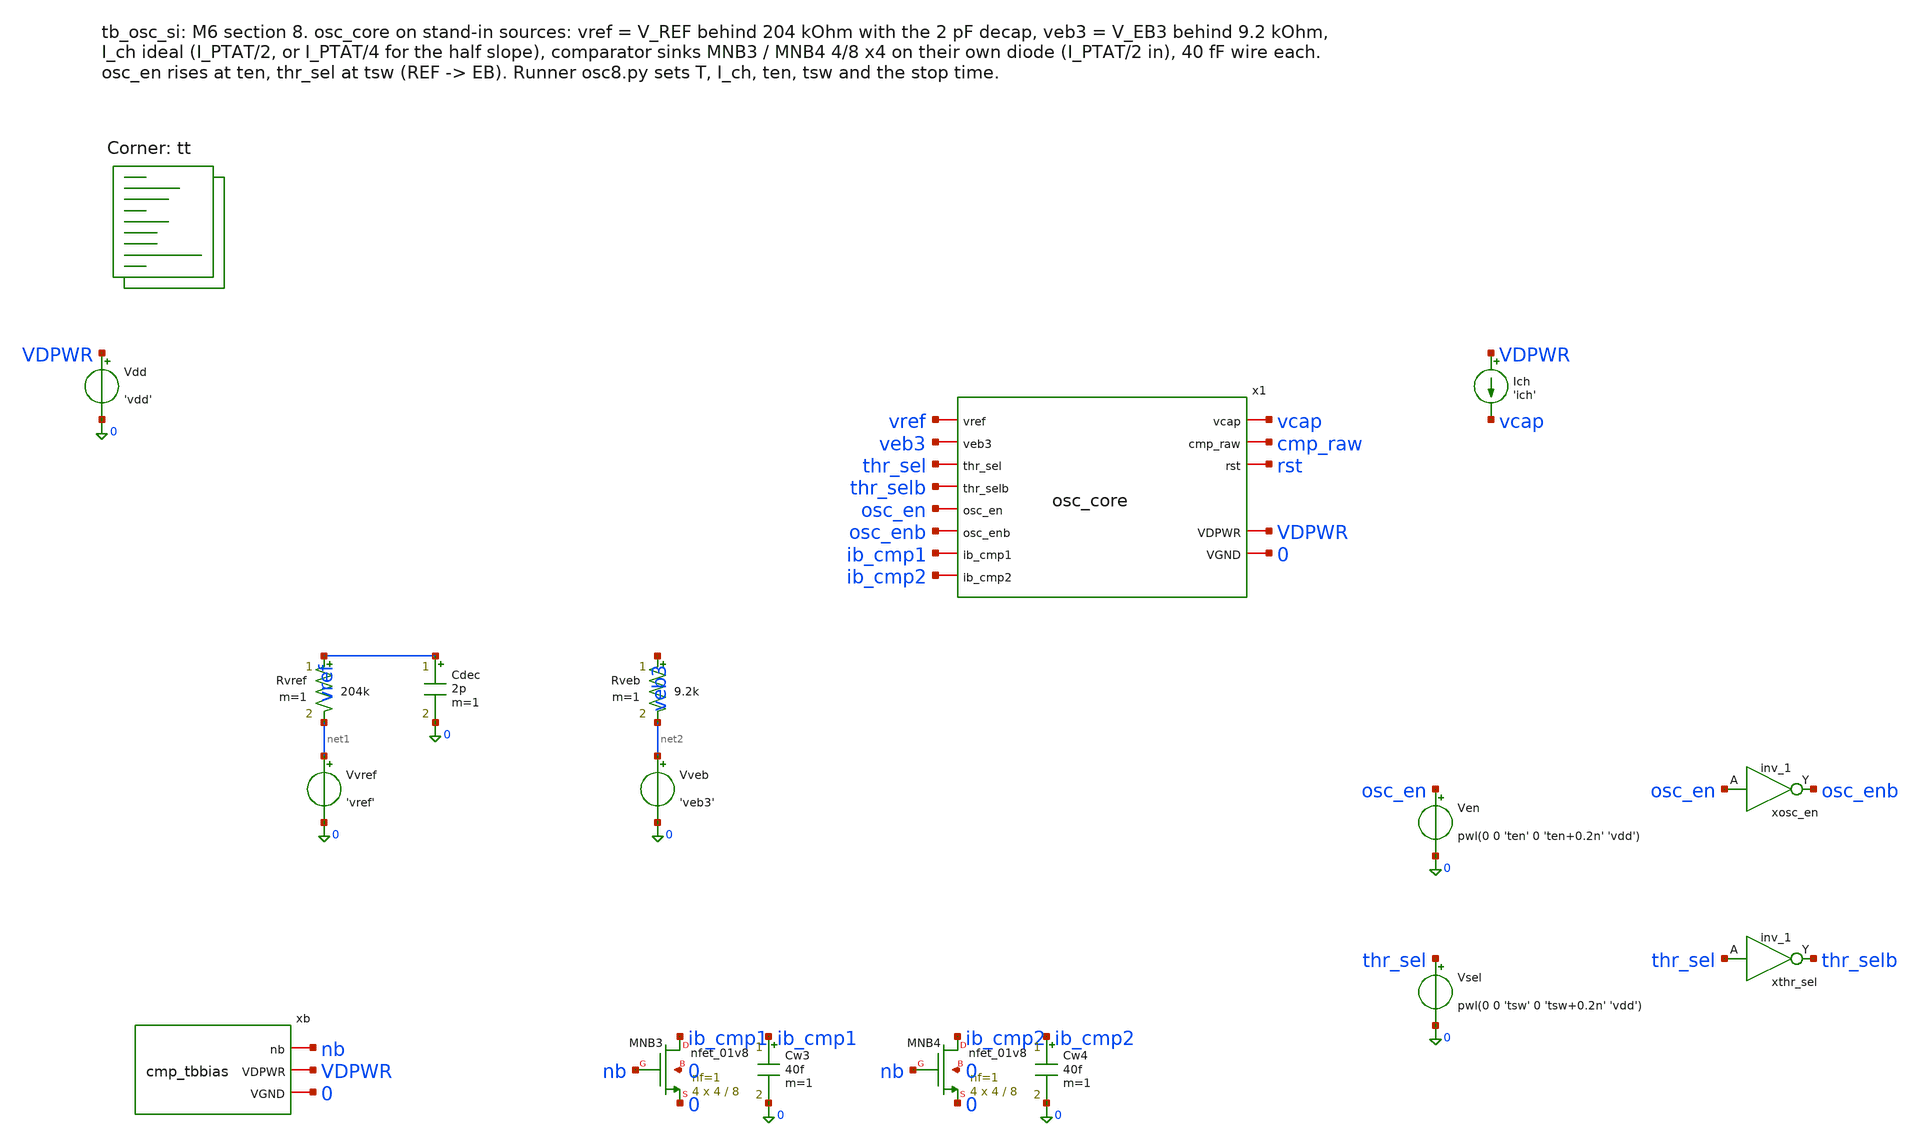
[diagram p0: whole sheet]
** sch_path: xschem/tb_osc_si.sch
**.subckt tb_osc_si
x1 vref veb3 thr_sel thr_selb osc_en osc_enb ib_cmp1 ib_cmp2 vcap cmp_raw rst VDPWR 0 osc_core
Ich VDPWR vcap 'ich'
Vdd VDPWR 0 'vdd'
Vvref net1 0 'vref'
Rvref vref net1 204k m=1
Cdec vref 0 2p m=1
Vveb net2 0 'veb3'
Rveb veb3 net2 9.2k m=1
xb nb VDPWR 0 cmp_tbbias
XMNB3 ib_cmp1 nb 0 0 sky130_fd_pr__nfet_01v8 L=8 W=4 nf=1 ad='int((1 + 1)/2) * 4 / 1 * 0.29' as='int((1 + 2)/2) * 4 / 1 * 0.29'
+ pd='2*int((1 + 1)/2) * (4 / 1 + 0.29)' ps='2*int((1 + 2)/2) * (4 / 1 + 0.29)' nrd='0.29 / 4 ' nrs='0.29 / 4 '
+ sa=0 sb=0 sd=0 mult=4 m=4
Cw3 ib_cmp1 0 40f m=1
XMNB4 ib_cmp2 nb 0 0 sky130_fd_pr__nfet_01v8 L=8 W=4 nf=1 ad='int((1 + 1)/2) * 4 / 1 * 0.29' as='int((1 + 2)/2) * 4 / 1 * 0.29'
+ pd='2*int((1 + 1)/2) * (4 / 1 + 0.29)' ps='2*int((1 + 2)/2) * (4 / 1 + 0.29)' nrd='0.29 / 4 ' nrs='0.29 / 4 '
+ sa=0 sb=0 sd=0 mult=4 m=4
Cw4 ib_cmp2 0 40f m=1
Ven osc_en 0 pwl(0 0 'ten' 0 'ten+0.2n' 'vdd')
xosc_en osc_en 0 0 VDPWR VDPWR osc_enb sky130_fd_sc_hd__inv_1
Vsel thr_sel 0 pwl(0 0 'tsw' 0 'tsw+0.2n' 'vdd')
xthr_sel thr_sel 0 0 VDPWR VDPWR thr_selb sky130_fd_sc_hd__inv_1
**** begin user architecture code
.lib $::SKYWATER_MODELS/sky130.lib.spice tt

.param vdd=1.8 vref=1.24324 veb3=0.709608 ich=1.385555u ten=2u tsw=65.3u
.include /foss/pdks/sky130A/libs.ref/sky130_fd_sc_hd/spice/sky130_fd_sc_hd.spice
.temp 25
.option method=gear
.control
save vcap x1.vthr rst cmp_raw x1.xos.sw
tran 0.2n 140u 0 0.2n
let tdr = 48u
let tde = 98u
meas tran r1 when v(rst)=0.9 rise=1
print r1
meas tran r2 when v(rst)=0.9 rise=2
print r2
meas tran r3 when v(rst)=0.9 rise=3
print r3
meas tran r4 when v(rst)=0.9 rise=4
print r4
meas tran r5 when v(rst)=0.9 rise=5
print r5
meas tran r6 when v(rst)=0.9 rise=6
print r6
meas tran r7 when v(rst)=0.9 rise=7
print r7
meas tran r8 when v(rst)=0.9 rise=8
print r8
meas tran r9 when v(rst)=0.9 rise=9
print r9
meas tran r10 when v(rst)=0.9 rise=10
print r10
meas tran r11 when v(rst)=0.9 rise=11
print r11
meas tran r12 when v(rst)=0.9 rise=12
print r12
meas tran r13 when v(rst)=0.9 rise=13
print r13
meas tran r14 when v(rst)=0.9 rise=14
print r14
meas tran r15 when v(rst)=0.9 rise=15
print r15
meas tran r16 when v(rst)=0.9 rise=16
print r16
meas tran r17 when v(rst)=0.9 rise=17
print r17
meas tran r18 when v(rst)=0.9 rise=18
print r18
meas tran r19 when v(rst)=0.9 rise=19
print r19
meas tran r20 when v(rst)=0.9 rise=20
print r20
meas tran r21 when v(rst)=0.9 rise=21
print r21
meas tran r22 when v(rst)=0.9 rise=22
print r22
meas tran r23 when v(rst)=0.9 rise=23
print r23
meas tran r24 when v(rst)=0.9 rise=24
print r24
meas tran r25 when v(rst)=0.9 rise=25
print r25
meas tran r26 when v(rst)=0.9 rise=26
print r26
meas tran r27 when v(rst)=0.9 rise=27
print r27
meas tran r28 when v(rst)=0.9 rise=28
print r28
meas tran r29 when v(rst)=0.9 rise=29
print r29
meas tran r30 when v(rst)=0.9 rise=30
print r30
meas tran r31 when v(rst)=0.9 rise=31
print r31
meas tran r32 when v(rst)=0.9 rise=32
print r32
meas tran tc when v(vcap)=v(x1.vthr) rise=1 td=$&tdr
meas tran tcmp when v(cmp_raw)=0.9 rise=1 td=$&tc
meas tran tswon when v(x1.xos.sw)=0.9 rise=1 td=$&tc
meas tran tswoff when v(x1.xos.sw)=0.9 fall=1 td=$&tc
meas tran vth find v(x1.vthr) at=$&tc
let tto = tswoff + 300n
meas tran vmin min v(vcap) from=$&tswoff to=$&tto
let dtd = tcmp - tc
let dlog = tswon - tcmp
let don = tswoff - tswon
let dtau = tswoff - tc
echo TAU ph=REF td=$&dtd tlog=$&dlog ton=$&don tau=$&dtau vth=$&vth vmin=$&vmin
meas tran tc when v(vcap)=v(x1.vthr) rise=1 td=$&tde
meas tran tcmp when v(cmp_raw)=0.9 rise=1 td=$&tc
meas tran tswon when v(x1.xos.sw)=0.9 rise=1 td=$&tc
meas tran tswoff when v(x1.xos.sw)=0.9 fall=1 td=$&tc
meas tran vth find v(x1.vthr) at=$&tc
let tto = tswoff + 300n
meas tran vmin min v(vcap) from=$&tswoff to=$&tto
let dtd = tcmp - tc
let dlog = tswon - tcmp
let don = tswoff - tswon
let dtau = tswoff - tc
echo TAU ph=EB td=$&dtd tlog=$&dlog ton=$&don tau=$&dtau vth=$&vth vmin=$&vmin
.endc

**** end user architecture code
**.ends

* expanding   symbol:  osc_core.sym # of pins=13
** sym_path: xschem/osc_core.sym
** sch_path: xschem/osc_core.sch
.subckt osc_core vref veb3 thr_sel thr_selb osc_en osc_enb ib_cmp1 ib_cmp2 vcap cmp_raw rst VDPWR
+ VGND
*.ipin vref
*.ipin veb3
*.ipin thr_sel
*.ipin thr_selb
*.iopin ib_cmp1
*.iopin ib_cmp2
*.opin cmp_raw
*.ipin osc_en
*.ipin osc_enb
*.iopin vcap
*.opin rst
*.iopin VDPWR
*.iopin VGND
xmux vref veb3 thr_sel thr_selb vthr VDPWR VGND thrmux
xcmp vthr vcap ib_cmp1 ib_cmp2 VDPWR cmp_raw VGND cmp2s
xos cmp_raw osc_en osc_enb vcap rst VDPWR VGND oneshot
XCosc vcap VGND sky130_fd_pr__cap_mim_m3_1 W=25 L=25 MF=4 m=4
.ends


* expanding   symbol:  cmp_tbbias.sym # of pins=3
** sym_path: xschem/cmp_tbbias.sym
** sch_path: xschem/cmp_tbbias.sch
.subckt cmp_tbbias nb VDPWR VGND
*.iopin VDPWR
*.iopin nb
*.iopin VGND
Iref VDPWR nb 1.386u
XMNB1 nb nb VGND VGND sky130_fd_pr__nfet_01v8 L=8 W=4 nf=1 ad='int((1 + 1)/2) * 4 / 1 * 0.29' as='int((1 + 2)/2) * 4 / 1 * 0.29'
+ pd='2*int((1 + 1)/2) * (4 / 1 + 0.29)' ps='2*int((1 + 2)/2) * (4 / 1 + 0.29)' nrd='0.29 / 4 ' nrs='0.29 / 4 '
+ sa=0 sb=0 sd=0 mult=1 m=1
.ends


* expanding   symbol:  thrmux.sym # of pins=7
** sym_path: xschem/thrmux.sym
** sch_path: xschem/thrmux.sch
.subckt thrmux vref veb3 thr_sel thr_selb vthr VDPWR VGND
*.ipin thr_sel
*.ipin thr_selb
*.ipin vref
*.ipin veb3
*.iopin vthr
*.iopin VDPWR
*.iopin VGND
xn1 thr_sel seb VGND VGND VDPWR VDPWR sref sky130_fd_sc_hd__nor2_1
xn2 sref thr_selb VGND VGND VDPWR VDPWR seb sky130_fd_sc_hd__nor2_1
xi1 sref VGND VGND VDPWR VDPWR srefb sky130_fd_sc_hd__inv_1
xi2 seb VGND VGND VDPWR VDPWR sebb sky130_fd_sc_hd__inv_1
XMTN1 vref sref vthr VGND sky130_fd_pr__nfet_01v8_lvt L=0.5 W=2 nf=1 ad='int((1 + 1)/2) * 2 / 1 * 0.29'
+ as='int((1 + 2)/2) * 2 / 1 * 0.29' pd='2*int((1 + 1)/2) * (2 / 1 + 0.29)' ps='2*int((1 + 2)/2) * (2 / 1 + 0.29)'
+ nrd='0.29 / 2 ' nrs='0.29 / 2 ' sa=0 sb=0 sd=0 mult=1 m=1
XMTP1 vthr srefb vref VDPWR sky130_fd_pr__pfet_01v8_lvt L=0.5 W=4 nf=1 ad='int((1 + 1)/2) * 4 / 1 * 0.29'
+ as='int((1 + 2)/2) * 4 / 1 * 0.29' pd='2*int((1 + 1)/2) * (4 / 1 + 0.29)' ps='2*int((1 + 2)/2) * (4 / 1 + 0.29)'
+ nrd='0.29 / 4 ' nrs='0.29 / 4 ' sa=0 sb=0 sd=0 mult=1 m=1
XMTN2 vthr seb veb3 VGND sky130_fd_pr__nfet_01v8_lvt L=0.5 W=2 nf=1 ad='int((1 + 1)/2) * 2 / 1 * 0.29'
+ as='int((1 + 2)/2) * 2 / 1 * 0.29' pd='2*int((1 + 1)/2) * (2 / 1 + 0.29)' ps='2*int((1 + 2)/2) * (2 / 1 + 0.29)'
+ nrd='0.29 / 2 ' nrs='0.29 / 2 ' sa=0 sb=0 sd=0 mult=1 m=1
XMTP2 veb3 sebb vthr VDPWR sky130_fd_pr__pfet_01v8_lvt L=0.5 W=4 nf=1 ad='int((1 + 1)/2) * 4 / 1 * 0.29'
+ as='int((1 + 2)/2) * 4 / 1 * 0.29' pd='2*int((1 + 1)/2) * (4 / 1 + 0.29)' ps='2*int((1 + 2)/2) * (4 / 1 + 0.29)'
+ nrd='0.29 / 4 ' nrs='0.29 / 4 ' sa=0 sb=0 sd=0 mult=1 m=1
.ends


* expanding   symbol:  cmp2s.sym # of pins=7
** sym_path: xschem/cmp2s.sym
** sch_path: xschem/cmp2s.sch
.subckt cmp2s vthr vcap ib_cmp1 ib_cmp2 VDPWR cmp_raw VGND
*.iopin VDPWR
*.iopin VGND
*.ipin vthr
*.ipin vcap
*.iopin ib_cmp1
*.iopin ib_cmp2
*.opin cmp_raw
XM2a nd nd VDPWR VDPWR sky130_fd_pr__pfet_01v8_lvt L=4 W=4 nf=1 ad='int((1 + 1)/2) * 4 / 1 * 0.29' as='int((1 + 2)/2) * 4 / 1 * 0.29'
+ pd='2*int((1 + 1)/2) * (4 / 1 + 0.29)' ps='2*int((1 + 2)/2) * (4 / 1 + 0.29)' nrd='0.29 / 4 ' nrs='0.29 / 4 '
+ sa=0 sb=0 sd=0 mult=8 m=8
XM2b n1 nd VDPWR VDPWR sky130_fd_pr__pfet_01v8_lvt L=4 W=4 nf=1 ad='int((1 + 1)/2) * 4 / 1 * 0.29' as='int((1 + 2)/2) * 4 / 1 * 0.29'
+ pd='2*int((1 + 1)/2) * (4 / 1 + 0.29)' ps='2*int((1 + 2)/2) * (4 / 1 + 0.29)' nrd='0.29 / 4 ' nrs='0.29 / 4 '
+ sa=0 sb=0 sd=0 mult=8 m=8
XM1a nd vthr ib_cmp1 VGND sky130_fd_pr__nfet_01v8_lvt L=1.75 W=10 nf=1 ad='int((1 + 1)/2) * 10 / 1 * 0.29'
+ as='int((1 + 2)/2) * 10 / 1 * 0.29' pd='2*int((1 + 1)/2) * (10 / 1 + 0.29)' ps='2*int((1 + 2)/2) * (10 / 1 + 0.29)'
+ nrd='0.29 / 10 ' nrs='0.29 / 10 ' sa=0 sb=0 sd=0 mult=6 m=6
XM1b n1 vcap ib_cmp1 VGND sky130_fd_pr__nfet_01v8_lvt L=1.75 W=10 nf=1 ad='int((1 + 1)/2) * 10 / 1 * 0.29'
+ as='int((1 + 2)/2) * 10 / 1 * 0.29' pd='2*int((1 + 1)/2) * (10 / 1 + 0.29)' ps='2*int((1 + 2)/2) * (10 / 1 + 0.29)'
+ nrd='0.29 / 10 ' nrs='0.29 / 10 ' sa=0 sb=0 sd=0 mult=6 m=6
XM3 ib_cmp2 n1 VDPWR VDPWR sky130_fd_pr__pfet_01v8_lvt L=1 W=4 nf=1 ad='int((1 + 1)/2) * 4 / 1 * 0.29'
+ as='int((1 + 2)/2) * 4 / 1 * 0.29' pd='2*int((1 + 1)/2) * (4 / 1 + 0.29)' ps='2*int((1 + 2)/2) * (4 / 1 + 0.29)'
+ nrd='0.29 / 4 ' nrs='0.29 / 4 ' sa=0 sb=0 sd=0 mult=3 m=3
XMIP x ib_cmp2 VDPWR VDPWR sky130_fd_pr__pfet_01v8 L=1 W=0.42 nf=1 ad='int((1 + 1)/2) * 0.42 / 1 * 0.29'
+ as='int((1 + 2)/2) * 0.42 / 1 * 0.29' pd='2*int((1 + 1)/2) * (0.42 / 1 + 0.29)' ps='2*int((1 + 2)/2) * (0.42 / 1 + 0.29)'
+ nrd='0.29 / 0.42 ' nrs='0.29 / 0.42 ' sa=0 sb=0 sd=0 mult=1 m=1
XMIN x ib_cmp2 VGND VGND sky130_fd_pr__nfet_01v8 L=0.15 W=2 nf=1 ad='int((1 + 1)/2) * 2 / 1 * 0.29' as='int((1 + 2)/2) * 2 / 1 * 0.29'
+ pd='2*int((1 + 1)/2) * (2 / 1 + 0.29)' ps='2*int((1 + 2)/2) * (2 / 1 + 0.29)' nrd='0.29 / 2 ' nrs='0.29 / 2 '
+ sa=0 sb=0 sd=0 mult=1 m=1
xinv x VGND VGND VDPWR VDPWR cmp_raw sky130_fd_sc_hd__inv_1
.ends


* expanding   symbol:  oneshot.sym # of pins=7
** sym_path: xschem/oneshot.sym
** sch_path: xschem/oneshot.sch
.subckt oneshot cmp_raw osc_en osc_enb vcap rst VDPWR VGND
*.ipin cmp_raw
*.ipin osc_enb
*.ipin osc_en
*.iopin vcap
*.opin rst
*.iopin VDPWR
*.iopin VGND
xbck cmp_raw VGND VGND VDPWR VDPWR ck sky130_fd_sc_hd__buf_2
xff ck VDPWR rb VGND VGND VDPWR VDPWR rst sky130_fd_sc_hd__dfrtp_1
xor rst osc_enb VGND VGND VDPWR VDPWR swp sky130_fd_sc_hd__or2_1
xi1 swp VGND VGND VDPWR VDPWR swn sky130_fd_sc_hd__inv_1
xand db osc_en VGND VGND VDPWR VDPWR rb sky130_fd_sc_hd__and2_1
xdl rst db VDPWR VGND dly5
XMDP sw swn VDPWR VDPWR sky130_fd_pr__pfet_01v8 L=0.15 W=2 nf=1 ad='int((1 + 1)/2) * 2 / 1 * 0.29' as='int((1 + 2)/2) * 2 / 1 * 0.29'
+ pd='2*int((1 + 1)/2) * (2 / 1 + 0.29)' ps='2*int((1 + 2)/2) * (2 / 1 + 0.29)' nrd='0.29 / 2 ' nrs='0.29 / 2 '
+ sa=0 sb=0 sd=0 mult=1 m=1
XMDN sw swn VGND VGND sky130_fd_pr__nfet_01v8 L=1.5 W=0.42 nf=1 ad='int((1 + 1)/2) * 0.42 / 1 * 0.29'
+ as='int((1 + 2)/2) * 0.42 / 1 * 0.29' pd='2*int((1 + 1)/2) * (0.42 / 1 + 0.29)' ps='2*int((1 + 2)/2) * (0.42 / 1 + 0.29)'
+ nrd='0.29 / 0.42 ' nrs='0.29 / 0.42 ' sa=0 sb=0 sd=0 mult=1 m=1
XMRST vcap sw VGND VGND sky130_fd_pr__nfet_01v8 L=0.5 W=6 nf=1 ad='int((1 + 1)/2) * 6 / 1 * 0.29' as='int((1 + 2)/2) * 6 / 1 * 0.29'
+ pd='2*int((1 + 1)/2) * (6 / 1 + 0.29)' ps='2*int((1 + 2)/2) * (6 / 1 + 0.29)' nrd='0.29 / 6 ' nrs='0.29 / 6 '
+ sa=0 sb=0 sd=0 mult=2 m=2
.ends


* expanding   symbol:  dly5.sym # of pins=4
** sym_path: xschem/dly5.sym
** sch_path: xschem/dly5.sch
.subckt dly5 a y VDPWR VGND
*.iopin VDPWR
*.iopin VGND
*.ipin a
*.opin y
XMP1 d1 a VDPWR VDPWR sky130_fd_pr__pfet_01v8 L=2.3 W=1 nf=1 ad='int((1 + 1)/2) * 1 / 1 * 0.29' as='int((1 + 2)/2) * 1 / 1 * 0.29'
+ pd='2*int((1 + 1)/2) * (1 / 1 + 0.29)' ps='2*int((1 + 2)/2) * (1 / 1 + 0.29)' nrd='0.29 / 1 ' nrs='0.29 / 1 '
+ sa=0 sb=0 sd=0 mult=1 m=1
XMN1 d1 a VGND VGND sky130_fd_pr__nfet_01v8 L=2.3 W=0.42 nf=1 ad='int((1 + 1)/2) * 0.42 / 1 * 0.29' as='int((1 + 2)/2) * 0.42 / 1 * 0.29'
+ pd='2*int((1 + 1)/2) * (0.42 / 1 + 0.29)' ps='2*int((1 + 2)/2) * (0.42 / 1 + 0.29)' nrd='0.29 / 0.42 '
+ nrs='0.29 / 0.42 ' sa=0 sb=0 sd=0 mult=1 m=1
XMP2 d2 d1 VDPWR VDPWR sky130_fd_pr__pfet_01v8 L=2.3 W=1 nf=1 ad='int((1 + 1)/2) * 1 / 1 * 0.29' as='int((1 + 2)/2) * 1 / 1 * 0.29'
+ pd='2*int((1 + 1)/2) * (1 / 1 + 0.29)' ps='2*int((1 + 2)/2) * (1 / 1 + 0.29)' nrd='0.29 / 1 ' nrs='0.29 / 1 '
+ sa=0 sb=0 sd=0 mult=1 m=1
XMN2 d2 d1 VGND VGND sky130_fd_pr__nfet_01v8 L=2.3 W=0.42 nf=1 ad='int((1 + 1)/2) * 0.42 / 1 * 0.29'
+ as='int((1 + 2)/2) * 0.42 / 1 * 0.29' pd='2*int((1 + 1)/2) * (0.42 / 1 + 0.29)' ps='2*int((1 + 2)/2) * (0.42 / 1 + 0.29)'
+ nrd='0.29 / 0.42 ' nrs='0.29 / 0.42 ' sa=0 sb=0 sd=0 mult=1 m=1
XMP3 d3 d2 VDPWR VDPWR sky130_fd_pr__pfet_01v8 L=2.3 W=1 nf=1 ad='int((1 + 1)/2) * 1 / 1 * 0.29' as='int((1 + 2)/2) * 1 / 1 * 0.29'
+ pd='2*int((1 + 1)/2) * (1 / 1 + 0.29)' ps='2*int((1 + 2)/2) * (1 / 1 + 0.29)' nrd='0.29 / 1 ' nrs='0.29 / 1 '
+ sa=0 sb=0 sd=0 mult=1 m=1
XMN3 d3 d2 VGND VGND sky130_fd_pr__nfet_01v8 L=2.3 W=0.42 nf=1 ad='int((1 + 1)/2) * 0.42 / 1 * 0.29'
+ as='int((1 + 2)/2) * 0.42 / 1 * 0.29' pd='2*int((1 + 1)/2) * (0.42 / 1 + 0.29)' ps='2*int((1 + 2)/2) * (0.42 / 1 + 0.29)'
+ nrd='0.29 / 0.42 ' nrs='0.29 / 0.42 ' sa=0 sb=0 sd=0 mult=1 m=1
XMP4 d4 d3 VDPWR VDPWR sky130_fd_pr__pfet_01v8 L=2.3 W=1 nf=1 ad='int((1 + 1)/2) * 1 / 1 * 0.29' as='int((1 + 2)/2) * 1 / 1 * 0.29'
+ pd='2*int((1 + 1)/2) * (1 / 1 + 0.29)' ps='2*int((1 + 2)/2) * (1 / 1 + 0.29)' nrd='0.29 / 1 ' nrs='0.29 / 1 '
+ sa=0 sb=0 sd=0 mult=1 m=1
XMN4 d4 d3 VGND VGND sky130_fd_pr__nfet_01v8 L=2.3 W=0.42 nf=1 ad='int((1 + 1)/2) * 0.42 / 1 * 0.29'
+ as='int((1 + 2)/2) * 0.42 / 1 * 0.29' pd='2*int((1 + 1)/2) * (0.42 / 1 + 0.29)' ps='2*int((1 + 2)/2) * (0.42 / 1 + 0.29)'
+ nrd='0.29 / 0.42 ' nrs='0.29 / 0.42 ' sa=0 sb=0 sd=0 mult=1 m=1
XMP5 y d4 VDPWR VDPWR sky130_fd_pr__pfet_01v8 L=2.3 W=1 nf=1 ad='int((1 + 1)/2) * 1 / 1 * 0.29' as='int((1 + 2)/2) * 1 / 1 * 0.29'
+ pd='2*int((1 + 1)/2) * (1 / 1 + 0.29)' ps='2*int((1 + 2)/2) * (1 / 1 + 0.29)' nrd='0.29 / 1 ' nrs='0.29 / 1 '
+ sa=0 sb=0 sd=0 mult=1 m=1
XMN5 y d4 VGND VGND sky130_fd_pr__nfet_01v8 L=2.3 W=0.42 nf=1 ad='int((1 + 1)/2) * 0.42 / 1 * 0.29' as='int((1 + 2)/2) * 0.42 / 1 * 0.29'
+ pd='2*int((1 + 1)/2) * (0.42 / 1 + 0.29)' ps='2*int((1 + 2)/2) * (0.42 / 1 + 0.29)' nrd='0.29 / 0.42 '
+ nrs='0.29 / 0.42 ' sa=0 sb=0 sd=0 mult=1 m=1
.ends

.end
